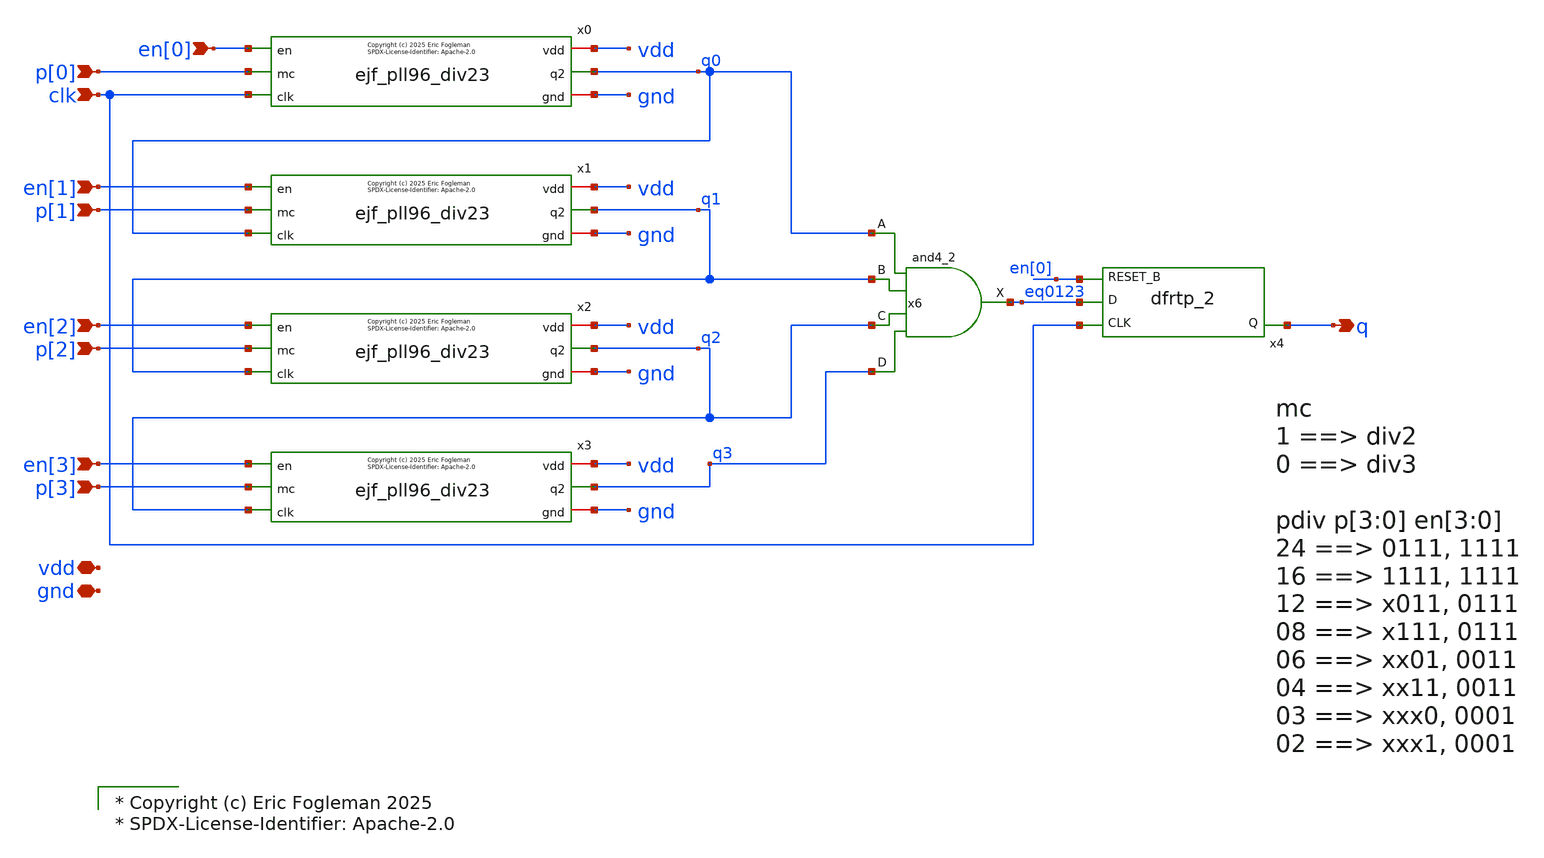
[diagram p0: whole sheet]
** sch_path: xschem/ejf_pll96_div_p.sch
* xschem/ejf_pll96_div23.sym:
* Copyright (c) 2025 Eric Fogleman

* Copyright (c) Eric Fogleman 2025
* SPDX-License-Identifier: Apache-2.0

**.subckt ejf_pll96_div_p vdd gnd clk p[1] p[2] p[3] en[3] en[2] q en[1] en[0] p[0]
*.iopin vdd
*.iopin gnd
*.ipin clk
*.ipin p[1]
*.ipin p[2]
*.ipin p[3]
*.ipin en[3]
*.ipin en[2]
*.opin q
*.ipin en[1]
*.ipin en[0]
*.ipin p[0]
x0 q0 clk p[0] vdd gnd en[0] ejf_pll96_div23
x1 q1 q0 p[1] vdd gnd en[1] ejf_pll96_div23
x2 q2 q1 p[2] vdd gnd en[2] ejf_pll96_div23
x3 q3 q2 p[3] vdd gnd en[3] ejf_pll96_div23
x6 q0 q1 q2 q3 gnd gnd vdd vdd eq0123 sky130_fd_sc_ls__and4_2
x4 clk eq0123 en[0] gnd gnd vdd vdd q sky130_fd_sc_ls__dfrtp_2
**.ends

* expanding   symbol:  ejf_pll96_div23.sym # of pins=6
** sym_path: xschem/ejf_pll96_div23.sym
** sch_path: xschem/ejf_pll96_div23.sch
.subckt ejf_pll96_div23 q2 clk mc vdd gnd en
*.ipin clk
*.ipin mc
*.opin q2
*.iopin vdd
*.iopin gnd
*.ipin en
x3 q1 mc net1 gnd gnd vdd vdd d2 sky130_fd_sc_ls__o21a_1
x1 clk net1 en gnd gnd vdd vdd q1 sky130_fd_sc_ls__dfstp_2
x2 clk d2 en gnd gnd vdd vdd q2 net1 sky130_fd_sc_ls__dfsbp_2
**** begin user architecture code

* Copyright (c) Eric Fogleman 2025
* SPDX-License-Identifier: Apache-2.0

**** end user architecture code
.ends

.end
